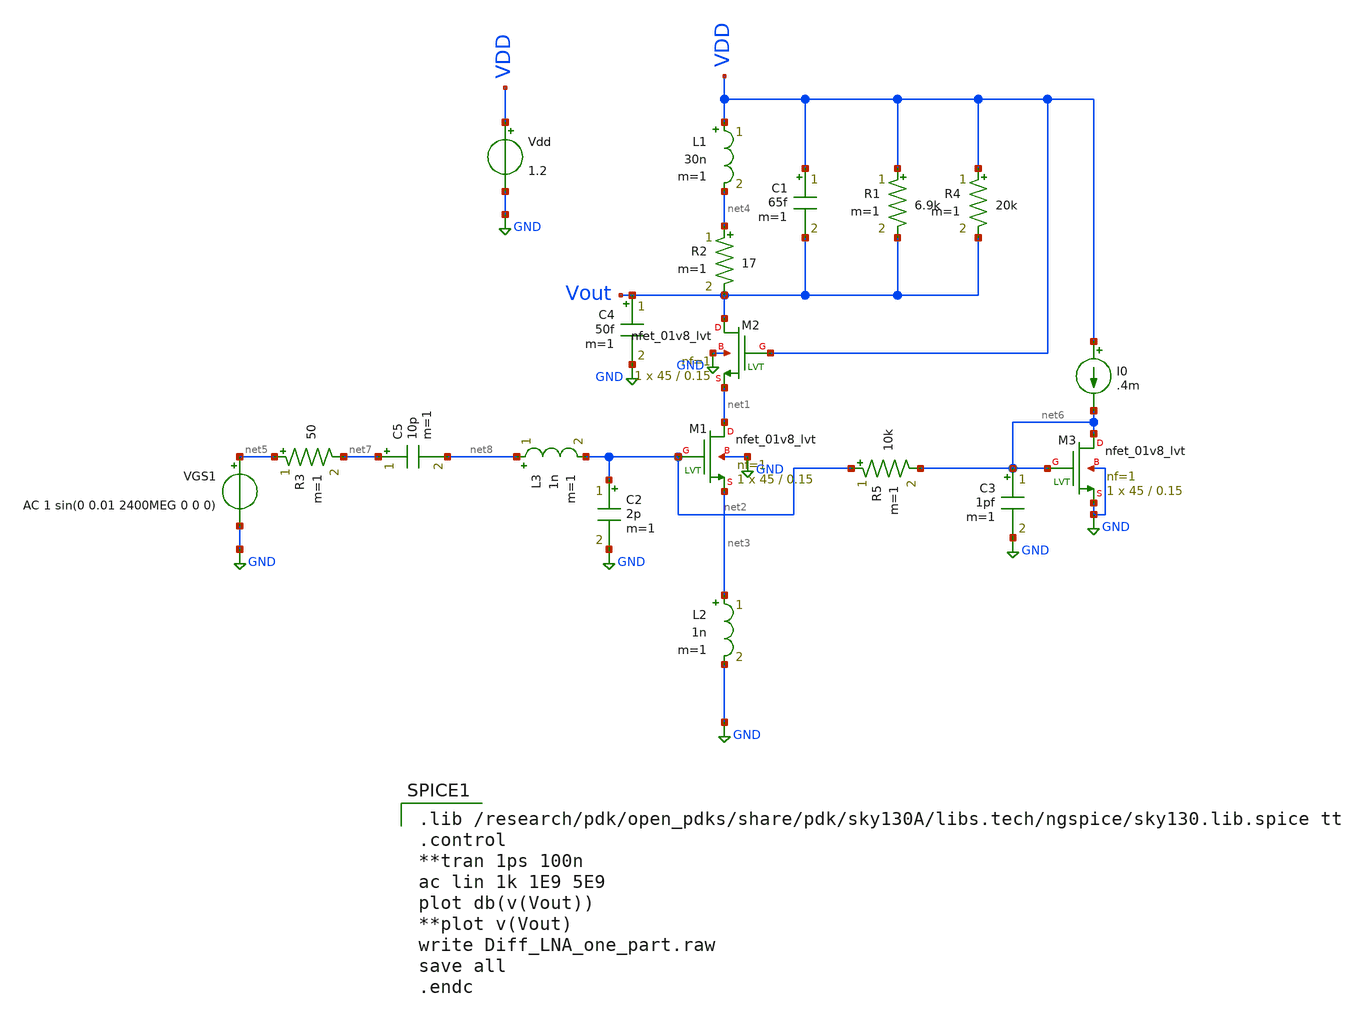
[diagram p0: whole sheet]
** sch_path: skywater_stuff/ECE631_RF_CMOS/Diff_LNA_one_part.sch
**.subckt Diff_LNA_one_part
XM1 net1 net2 net3 GND sky130_fd_pr__nfet_01v8_lvt L=0.15 W=45 nf=1 ad='int((nf+1)/2) * W/nf * 0.29'
+ as='int((nf+2)/2) * W/nf * 0.29' pd='2*int((nf+1)/2) * (W/nf + 0.29)' ps='2*int((nf+2)/2) * (W/nf + 0.29)'
+ nrd='0.29 / W' nrs='0.29 / W' sa=0 sb=0 sd=0 mult=1 m=1
L1 VDD net4 30n m=1
Vdd VDD GND 1.2
XM2 Vout VDD net1 GND sky130_fd_pr__nfet_01v8_lvt L=0.15 W=45 nf=1 ad='int((nf+1)/2) * W/nf * 0.29' as='int((nf+2)/2) * W/nf * 0.29'
+ pd='2*int((nf+1)/2) * (W/nf + 0.29)' ps='2*int((nf+2)/2) * (W/nf + 0.29)' nrd='0.29 / W' nrs='0.29 / W'
+ sa=0 sb=0 sd=0 mult=1 m=1
VGS1 net5 GND AC 1 sin(0 0.01 2400MEG 0 0 0)
C1 VDD Vout 65f m=1
L2 net3 GND 1n m=1
R1 VDD Vout 6.9k m=1
R2 net4 Vout 17 m=1
R3 net5 net7 50 m=1
C2 net2 GND 2p m=1
I0 VDD net6 .4m
XM3 net6 net6 GND GND sky130_fd_pr__nfet_01v8_lvt L=0.15 W=45 nf=1 ad='int((nf+1)/2) * W/nf * 0.29' as='int((nf+2)/2) * W/nf * 0.29'
+ pd='2*int((nf+1)/2) * (W/nf + 0.29)' ps='2*int((nf+2)/2) * (W/nf + 0.29)' nrd='0.29 / W' nrs='0.29 / W'
+ sa=0 sb=0 sd=0 mult=1 m=1
L3 net8 net2 1n m=1
C4 Vout GND 50f m=1
R4 VDD Vout 20k m=1
R5 net2 net6 10k m=1
C3 net6 GND 1pf m=1
C5 net7 net8 10p m=1
**** begin user architecture code

.lib /research/pdk/open_pdks/share/pdk/sky130A/libs.tech/ngspice/sky130.lib.spice tt
.control
**tran 1ps 100n
ac lin 1k 1E9 5E9
plot db(v(Vout))
**plot v(Vout)
write Diff_LNA_one_part.raw
save all
.endc


**** end user architecture code
**.ends
.GLOBAL GND
.end
